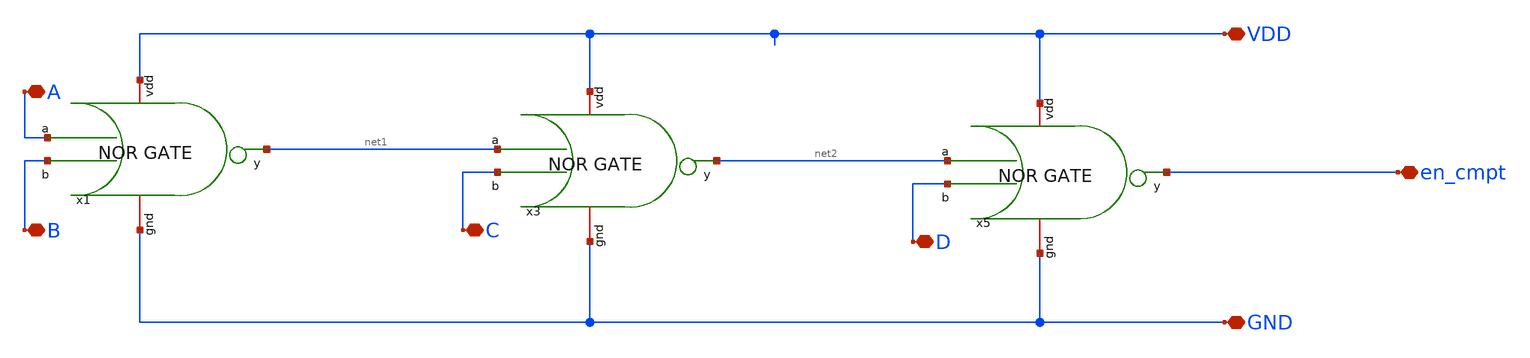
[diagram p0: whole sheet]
** sch_path: src/schematic/EN-COMPUTE/en_compute.sch
**.subckt en_compute VDD GND en_cmpt D C B A
*.iopin VDD
*.iopin GND
*.iopin en_cmpt
*.iopin D
*.iopin C
*.iopin B
*.iopin A
x1 VDD A B net1 GND norGate
x3 VDD net1 C net2 GND norGate
x5 VDD net2 D en_cmpt GND norGate
**.ends

* expanding   symbol:  src/schematic/NOR/norGate.sym # of pins=5
** sym_path: src/schematic/EN-COMPUTE/norGate.sym
** sch_path: src/schematic/EN-COMPUTE/norGate.sch
.subckt norGate vdd a b y gnd
*.iopin gnd
*.iopin vdd
*.ipin a
*.ipin b
*.opin y
XM1 y a net1 vdd pfet_03v3 L=0.28u W=0.22u nf=1 ad='int((nf+1)/2) * W/nf * 0.18u' as='int((nf+2)/2) * W/nf * 0.18u'
+ pd='2*int((nf+1)/2) * (W/nf + 0.18u)' ps='2*int((nf+2)/2) * (W/nf + 0.18u)' nrd='0.18u / W' nrs='0.18u / W'
+ sa=0 sb=0 sd=0 m=1
XM2 net1 a vdd vdd pfet_03v3 L=0.28u W=0.22u nf=1 ad='int((nf+1)/2) * W/nf * 0.18u' as='int((nf+2)/2) * W/nf * 0.18u'
+ pd='2*int((nf+1)/2) * (W/nf + 0.18u)' ps='2*int((nf+2)/2) * (W/nf + 0.18u)' nrd='0.18u / W' nrs='0.18u / W'
+ sa=0 sb=0 sd=0 m=1
XM3 y a gnd gnd nfet_03v3 L=0.28u W=0.22u nf=1 ad='int((nf+1)/2) * W/nf * 0.18u' as='int((nf+2)/2) * W/nf * 0.18u'
+ pd='2*int((nf+1)/2) * (W/nf + 0.18u)' ps='2*int((nf+2)/2) * (W/nf + 0.18u)' nrd='0.18u / W' nrs='0.18u / W'
+ sa=0 sb=0 sd=0 m=1
XM4 y a gnd gnd nfet_03v3 L=0.28u W=0.22u nf=1 ad='int((nf+1)/2) * W/nf * 0.18u' as='int((nf+2)/2) * W/nf * 0.18u'
+ pd='2*int((nf+1)/2) * (W/nf + 0.18u)' ps='2*int((nf+2)/2) * (W/nf + 0.18u)' nrd='0.18u / W' nrs='0.18u / W'
+ sa=0 sb=0 sd=0 m=1
.ends

.end
